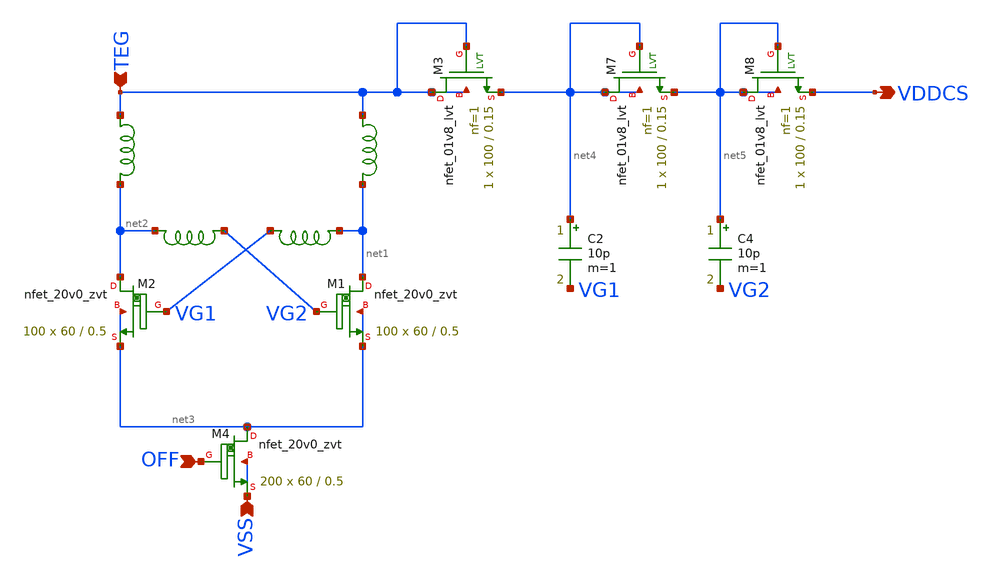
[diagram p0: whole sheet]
** sch_path: design/LELO_SVOD_SKY130A/LELO_COLD_START.sch
**.subckt LELO_COLD_START VSS TEG VDDCS OFF
*.ipin VSS
*.ipin TEG
*.opin VDDCS
*.ipin OFF
C2 net4 VG1 10p m=1
x1 VG2 net2 1812PS-564_imp
x2 net1 VG1 1812PS-564_imp
C4 net5 VG2 10p m=1
XM1 net1 VG2 net3 net3 sky130_fd_pr__nfet_20v0_zvt W=60 L=0.5 m=100
XM2 net2 VG1 net3 net3 sky130_fd_pr__nfet_20v0_zvt W=60 L=0.5 m=100
XM3 TEG TEG net4 TEG sky130_fd_pr__nfet_01v8_lvt L=0.15 W=100 nf=1 ad='int((1 + 1)/2) * 100 / 1 * 0.29'
+ as='int((1 + 2)/2) * 100 / 1 * 0.29' pd='2*int((1 + 1)/2) * (100 / 1 + 0.29)' ps='2*int((1 + 2)/2) * (100 / 1 + 0.29)'
+ nrd='0.29 / 100 ' nrs='0.29 / 100 ' sa=0 sb=0 sd=0 mult=1 m=1
XM7 net4 net4 net5 net4 sky130_fd_pr__nfet_01v8_lvt L=0.15 W=100 nf=1 ad='int((1 + 1)/2) * 100 / 1 * 0.29'
+ as='int((1 + 2)/2) * 100 / 1 * 0.29' pd='2*int((1 + 1)/2) * (100 / 1 + 0.29)' ps='2*int((1 + 2)/2) * (100 / 1 + 0.29)'
+ nrd='0.29 / 100 ' nrs='0.29 / 100 ' sa=0 sb=0 sd=0 mult=1 m=1
XM8 net5 net5 VDDCS net5 sky130_fd_pr__nfet_01v8_lvt L=0.15 W=100 nf=1 ad='int((1 + 1)/2) * 100 / 1 * 0.29'
+ as='int((1 + 2)/2) * 100 / 1 * 0.29' pd='2*int((1 + 1)/2) * (100 / 1 + 0.29)' ps='2*int((1 + 2)/2) * (100 / 1 + 0.29)'
+ nrd='0.29 / 100 ' nrs='0.29 / 100 ' sa=0 sb=0 sd=0 mult=1 m=1
XM4 net3 OFF VSS VSS sky130_fd_pr__nfet_20v0_zvt W=60 L=0.5 m=200
x3 TEG net2 XGL6030-103_sat
x4 TEG net1 XGL6030-103_sat
**.ends

* expanding   symbol:  LELO_SVOD_SKY130A/1812PS-564_imp.sym # of pins=2
** sym_path: design/LELO_SVOD_SKY130A/1812PS-564_imp.sym

.subckt 1812PS-564_imp port1 port2
X1 port1 port2 Model1D R1=70 R2=6.1 C= 7.71p K1=0.000001 K2=115.8 K3= 560u K4=0.000001 K5=0.000001
+ L=0 Is=0 a=0 L_Z0=0 L_EL=0 L_F0=0E6 PkZ=153558.837
.ends 1812PS-564_imp

* expanding   symbol:  LELO_SVOD_SKY130A/XGL6030-103_sat.sym # of pins=2
** sym_path: design/LELO_SVOD_SKY130A/XGL6030-103_sat.sym

.subckt XGL6030-103_sat port1 port2
X1 port1 port2 Model1C R1=5 R2=0.044 C= 14p K1=0.000001 K2=2.04 K3= 10u K4=0.000001 K5=0.000001
+ L=8.6548E-06 Is=10.3166 a=1.1241 L_Z0=0 L_EL=0 L_F0=0E6 PkZ=7109.28917
.ends XGL6030-103_sat
.end
